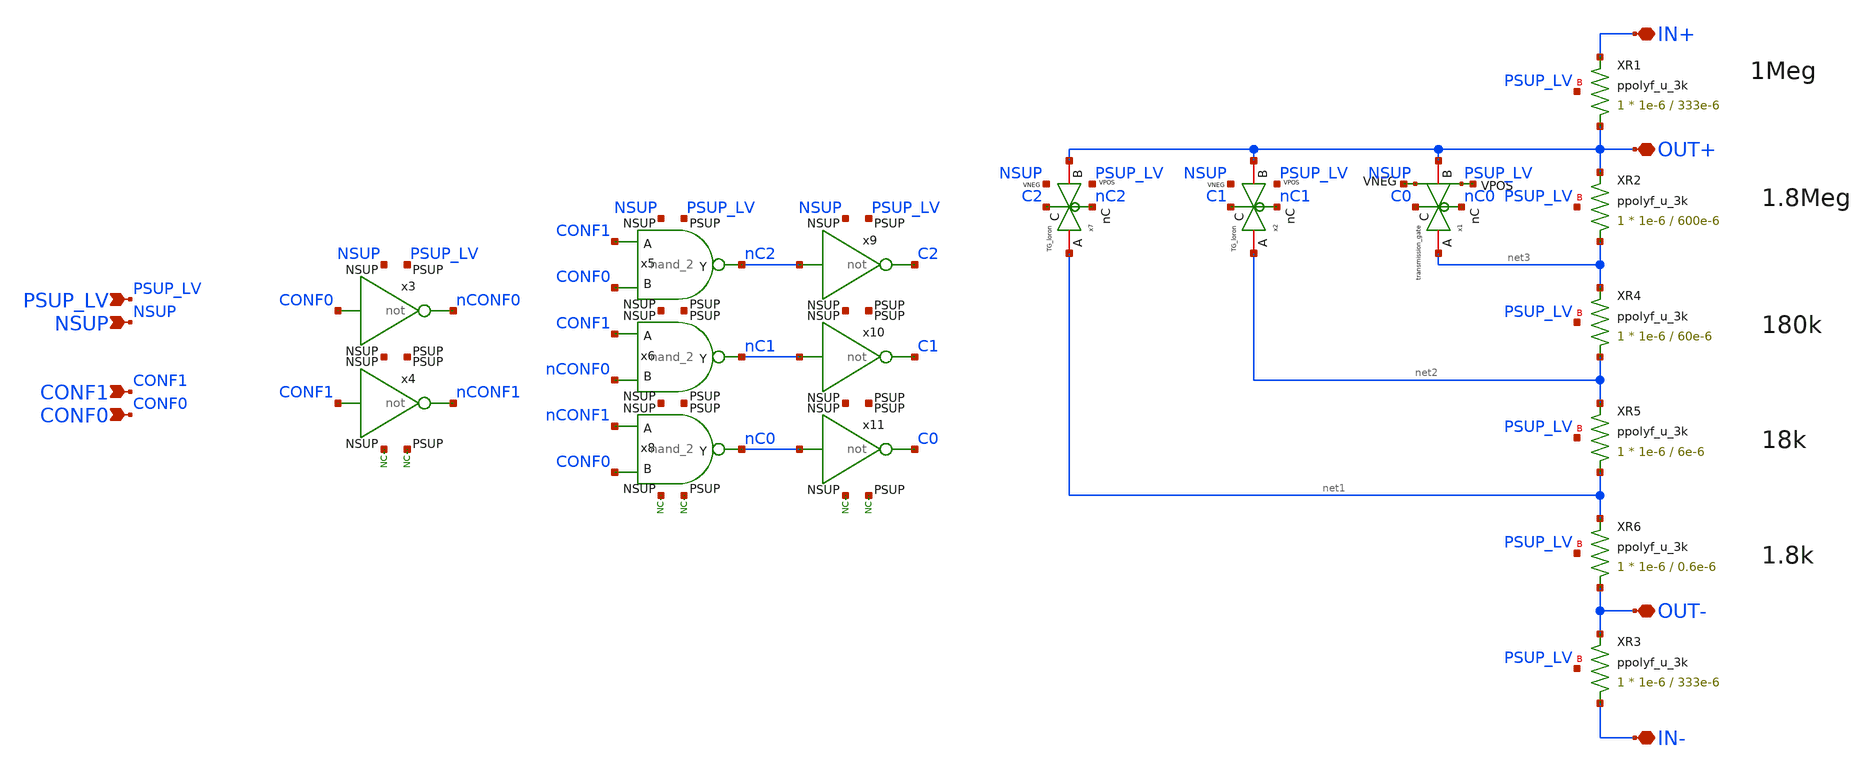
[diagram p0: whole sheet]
** sch_path: xschem/blocks/INA_gain_fb/INA_gain_fb.sch
**.subckt INA_gain_fb IN+ IN- OUT- OUT+ PSUP_LV NSUP CONF0 CONF1
*.iopin IN+
*.iopin IN-
*.iopin OUT-
*.iopin OUT+
*.ipin PSUP_LV
*.ipin NSUP
*.ipin CONF0
*.ipin CONF1
XR1 OUT+ IN+ PSUP_LV ppolyf_u_3k r_width=1e-6 r_length=333e-6 m=1
XR2 net3 OUT+ PSUP_LV ppolyf_u_3k r_width=1e-6 r_length=600e-6 m=1
XR3 IN- OUT- PSUP_LV ppolyf_u_3k r_width=1e-6 r_length=333e-6 m=1
x1 C0 net3 OUT+ nC0 net4 net5 transmission_gate
XR4 net2 net3 PSUP_LV ppolyf_u_3k r_width=1e-6 r_length=60e-6 m=1
XR5 net1 net2 PSUP_LV ppolyf_u_3k r_width=1e-6 r_length=6e-6 m=1
XR6 OUT- net1 PSUP_LV ppolyf_u_3k r_width=1e-6 r_length=0.6e-6 m=1
* noconn NSUP
* noconn PSUP_LV
x7 C2 net1 OUT+ nC2 PSUP_LV NSUP TG_loron
x2 C1 net2 OUT+ nC1 PSUP_LV NSUP TG_loron
x3 PSUP_LV CONF0 nCONF0 NSUP not
x4 PSUP_LV CONF1 nCONF1 NSUP not
x5 nC2 CONF1 CONF0 PSUP_LV NSUP nand_2
x6 nC1 CONF1 nCONF0 PSUP_LV NSUP nand_2
x8 nC0 nCONF1 CONF0 PSUP_LV NSUP nand_2
* noconn NSUP
* noconn PSUP_LV
x9 PSUP_LV nC2 C2 NSUP not
x10 PSUP_LV nC1 C1 NSUP not
x11 PSUP_LV nC0 C0 NSUP not
* noconn NSUP
* noconn PSUP_LV
**.ends

* expanding   symbol:  blocks/transmission_gate/transmission_gate.sym # of pins=6
** sym_path: xschem/blocks/transmission_gate/transmission_gate.sym
** sch_path: xschem/blocks/transmission_gate/transmission_gate.sch
.subckt transmission_gate C A B nC VPOS VNEG
*.iopin A
*.iopin B
*.ipin C
*.ipin nC
*.ipin VPOS
*.ipin VNEG
XM3 A C B VNEG nfet_03v3 L=2u W=10u nf=1 ad='int((nf+1)/2) * W/nf * 0.18u' as='int((nf+2)/2) * W/nf * 0.18u'
+ pd='2*int((nf+1)/2) * (W/nf + 0.18u)' ps='2*int((nf+2)/2) * (W/nf + 0.18u)' nrd='0.18u / W' nrs='0.18u / W'
+ sa=0 sb=0 sd=0 m=2
XM4 A nC B VPOS pfet_03v3 L=2u W=10u nf=1 ad='int((nf+1)/2) * W/nf * 0.18u' as='int((nf+2)/2) * W/nf * 0.18u'
+ pd='2*int((nf+1)/2) * (W/nf + 0.18u)' ps='2*int((nf+2)/2) * (W/nf + 0.18u)' nrd='0.18u / W' nrs='0.18u / W'
+ sa=0 sb=0 sd=0 m=4
.ends


* expanding   symbol:  blocks/TG_loron/TG_loron.sym # of pins=6
** sym_path: xschem/blocks/TG_loron/TG_loron.sym
** sch_path: xschem/blocks/TG_loron/TG_loron.sch
.subckt TG_loron C A B nC VPOS VNEG
*.iopin A
*.iopin B
*.ipin C
*.ipin nC
*.ipin VPOS
*.ipin VNEG
XM3 A C B VNEG nfet_03v3 L=2u W=10u nf=1 ad='int((nf+1)/2) * W/nf * 0.18u' as='int((nf+2)/2) * W/nf * 0.18u'
+ pd='2*int((nf+1)/2) * (W/nf + 0.18u)' ps='2*int((nf+2)/2) * (W/nf + 0.18u)' nrd='0.18u / W' nrs='0.18u / W'
+ sa=0 sb=0 sd=0 m=8
XM4 A nC B VPOS pfet_03v3 L=2u W=10u nf=1 ad='int((nf+1)/2) * W/nf * 0.18u' as='int((nf+2)/2) * W/nf * 0.18u'
+ pd='2*int((nf+1)/2) * (W/nf + 0.18u)' ps='2*int((nf+2)/2) * (W/nf + 0.18u)' nrd='0.18u / W' nrs='0.18u / W'
+ sa=0 sb=0 sd=0 m=16
.ends


* expanding   symbol:  blocks/not/not.sym # of pins=6
** sym_path: xschem/blocks/not/not.sym
** sch_path: xschem/blocks/not/not.sch
.subckt not PSUP A B NSUP
*.ipin PSUP
*.ipin NSUP
*.ipin A
*.opin B
XM2 B A NSUP NSUP nfet_03v3 L=0.28u W=0.22u nf=1 ad='int((nf+1)/2) * W/nf * 0.18u' as='int((nf+2)/2) * W/nf * 0.18u'
+ pd='2*int((nf+1)/2) * (W/nf + 0.18u)' ps='2*int((nf+2)/2) * (W/nf + 0.18u)' nrd='0.18u / W' nrs='0.18u / W'
+ sa=0 sb=0 sd=0 m=1
XM1 B A PSUP PSUP pfet_03v3 L=0.28u W=0.5u nf=1 ad='int((nf+1)/2) * W/nf * 0.18u' as='int((nf+2)/2) * W/nf * 0.18u'
+ pd='2*int((nf+1)/2) * (W/nf + 0.18u)' ps='2*int((nf+2)/2) * (W/nf + 0.18u)' nrd='0.18u / W' nrs='0.18u / W'
+ sa=0 sb=0 sd=0 m=1
.ends


* expanding   symbol:  blocks/nand_2/nand_2.sym # of pins=7
** sym_path: xschem/blocks/nand_2/nand_2.sym
** sch_path: xschem/blocks/nand_2/nand_2.sch
.subckt nand_2 Y A B PSUP NSUP
*.ipin PSUP
*.ipin NSUP
*.ipin A
*.ipin B
*.opin Y
XM5 net1 B NSUP NSUP nfet_03v3 L=0.28u W=0.22u nf=1 ad='int((nf+1)/2) * W/nf * 0.18u' as='int((nf+2)/2) * W/nf * 0.18u'
+ pd='2*int((nf+1)/2) * (W/nf + 0.18u)' ps='2*int((nf+2)/2) * (W/nf + 0.18u)' nrd='0.18u / W' nrs='0.18u / W'
+ sa=0 sb=0 sd=0 m=1
XM1 Y A net1 NSUP nfet_03v3 L=0.28u W=0.22u nf=1 ad='int((nf+1)/2) * W/nf * 0.18u' as='int((nf+2)/2) * W/nf * 0.18u'
+ pd='2*int((nf+1)/2) * (W/nf + 0.18u)' ps='2*int((nf+2)/2) * (W/nf + 0.18u)' nrd='0.18u / W' nrs='0.18u / W'
+ sa=0 sb=0 sd=0 m=1
XM2 Y A PSUP PSUP pfet_03v3 L=0.28u W=0.5u nf=1 ad='int((nf+1)/2) * W/nf * 0.18u' as='int((nf+2)/2) * W/nf * 0.18u'
+ pd='2*int((nf+1)/2) * (W/nf + 0.18u)' ps='2*int((nf+2)/2) * (W/nf + 0.18u)' nrd='0.18u / W' nrs='0.18u / W'
+ sa=0 sb=0 sd=0 m=1
XM3 Y B PSUP PSUP pfet_03v3 L=0.28u W=0.5u nf=1 ad='int((nf+1)/2) * W/nf * 0.18u' as='int((nf+2)/2) * W/nf * 0.18u'
+ pd='2*int((nf+1)/2) * (W/nf + 0.18u)' ps='2*int((nf+2)/2) * (W/nf + 0.18u)' nrd='0.18u / W' nrs='0.18u / W'
+ sa=0 sb=0 sd=0 m=1
.ends

.end
